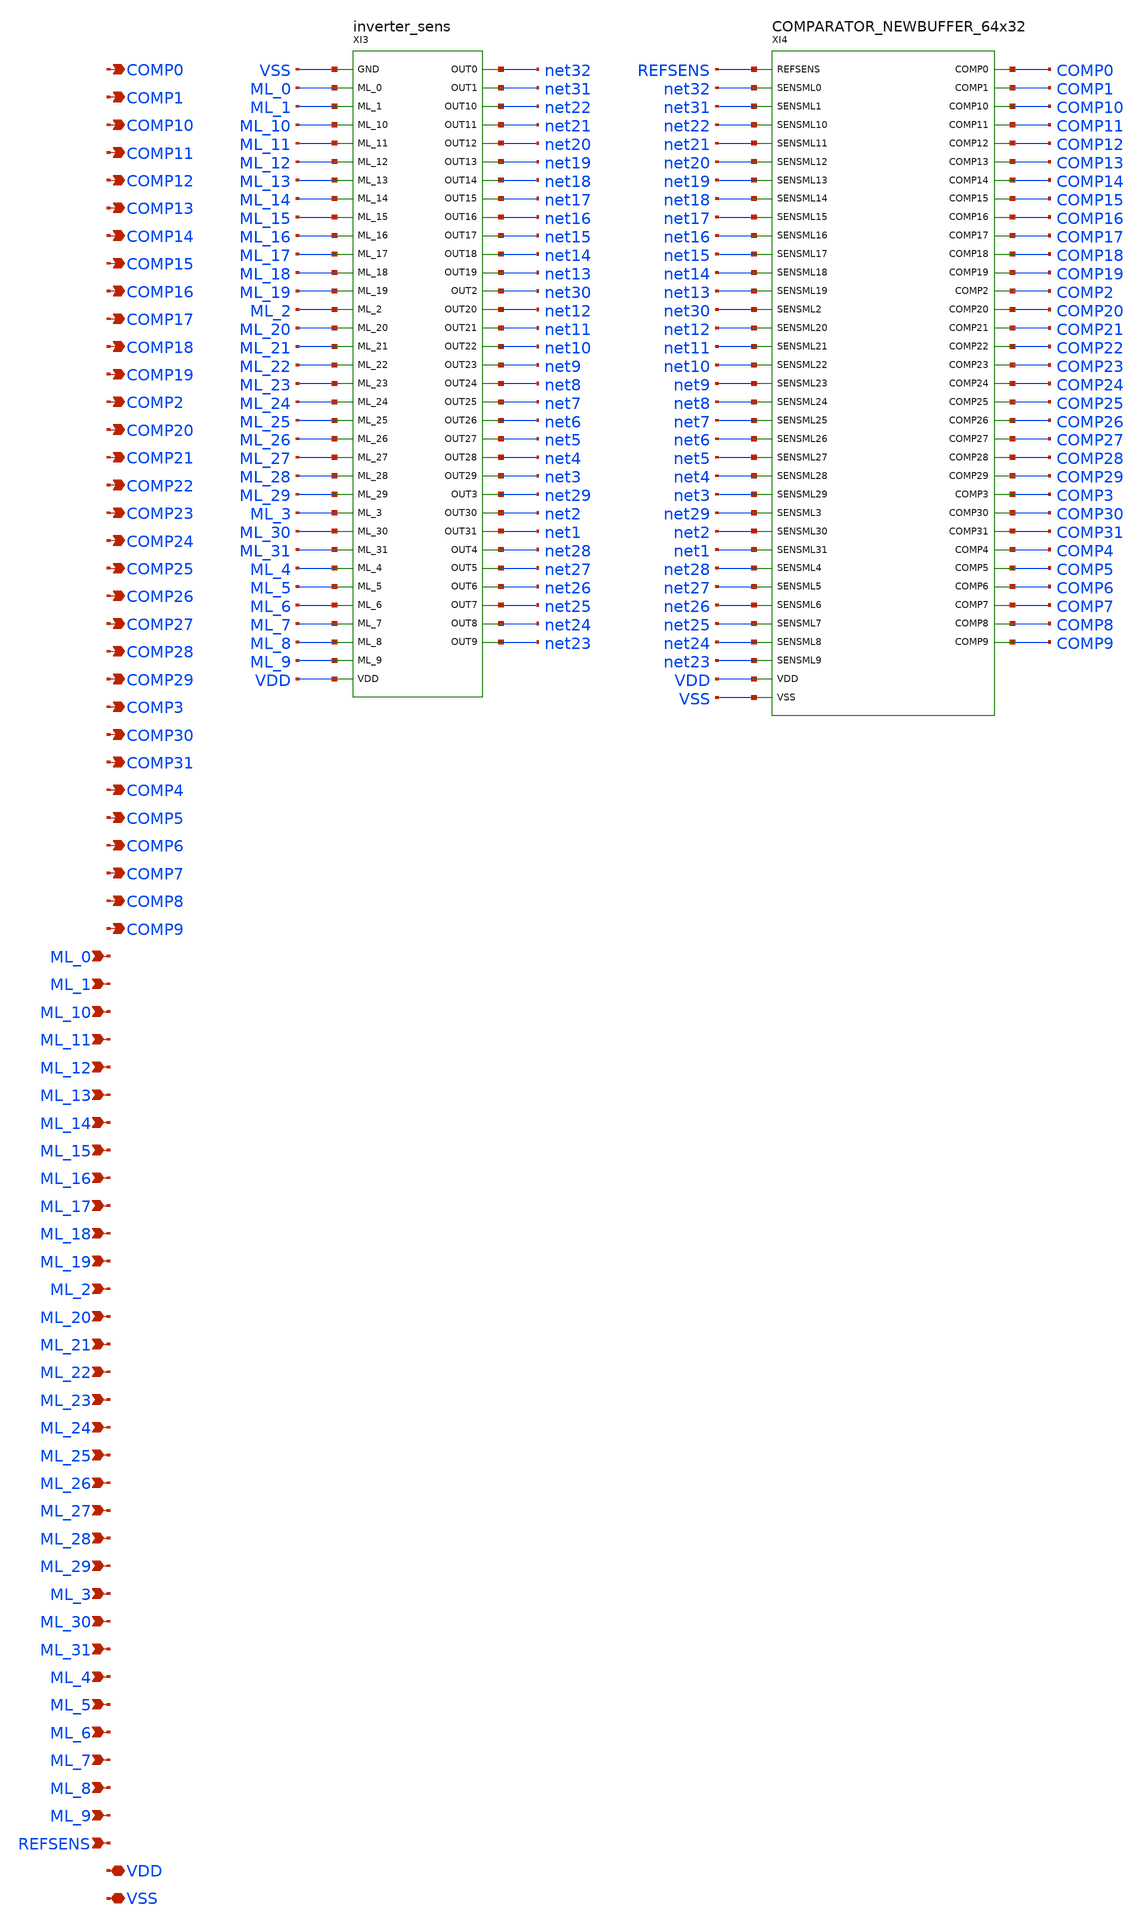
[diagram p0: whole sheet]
** sch_path: SoC6169-main/schematic/xschem/PART_SENS_COMPARATOR.sch
* Copyright 2026 USFQ CAM team
* Licensed under the Apache License, Version 2.0 (the "License");
* you may not use this file except in compliance with the License.
* You may obtain a copy of the License at
* https://www.apache.org/licenses/LICENSE-2.0
* Unless required by applicable law or agreed to in writing, software
* distributed under the License is distributed on an "AS IS" BASIS,
* WITHOUT WARRANTIES OR CONDITIONS OF ANY KIND, either express or implied.
* See the License for the specific language governing permissions and
* limitations under the License.
**.subckt PART_SENS_COMPARATOR COMP0 COMP1 COMP10 COMP11 COMP12 COMP13 COMP14 COMP15 COMP16 COMP17
*+ COMP18 COMP19 COMP2 COMP20 COMP21 COMP22 COMP23 COMP24 COMP25 COMP26 COMP27 COMP28 COMP29 COMP3 COMP30
*+ COMP31 COMP4 COMP5 COMP6 COMP7 COMP8 COMP9 ML_0 ML_1 ML_10 ML_11 ML_12 ML_13 ML_14 ML_15 ML_16 ML_17 ML_18
*+ ML_19 ML_2 ML_20 ML_21 ML_22 ML_23 ML_24 ML_25 ML_26 ML_27 ML_28 ML_29 ML_3 ML_30 ML_31 ML_4 ML_5 ML_6
*+ ML_7 ML_8 ML_9 REFSENS VDD VSS
*.opin COMP0
*.opin COMP1
*.opin COMP10
*.opin COMP11
*.opin COMP12
*.opin COMP13
*.opin COMP14
*.opin COMP15
*.opin COMP16
*.opin COMP17
*.opin COMP18
*.opin COMP19
*.opin COMP2
*.opin COMP20
*.opin COMP21
*.opin COMP22
*.opin COMP23
*.opin COMP24
*.opin COMP25
*.opin COMP26
*.opin COMP27
*.opin COMP28
*.opin COMP29
*.opin COMP3
*.opin COMP30
*.opin COMP31
*.opin COMP4
*.opin COMP5
*.opin COMP6
*.opin COMP7
*.opin COMP8
*.opin COMP9
*.ipin ML_0
*.ipin ML_1
*.ipin ML_10
*.ipin ML_11
*.ipin ML_12
*.ipin ML_13
*.ipin ML_14
*.ipin ML_15
*.ipin ML_16
*.ipin ML_17
*.ipin ML_18
*.ipin ML_19
*.ipin ML_2
*.ipin ML_20
*.ipin ML_21
*.ipin ML_22
*.ipin ML_23
*.ipin ML_24
*.ipin ML_25
*.ipin ML_26
*.ipin ML_27
*.ipin ML_28
*.ipin ML_29
*.ipin ML_3
*.ipin ML_30
*.ipin ML_31
*.ipin ML_4
*.ipin ML_5
*.ipin ML_6
*.ipin ML_7
*.ipin ML_8
*.ipin ML_9
*.ipin REFSENS
*.iopin VDD
*.iopin VSS
XI3 VSS ML_0 ML_1 ML_10 ML_11 ML_12 ML_13 ML_14 ML_15 ML_16 ML_17 ML_18 ML_19 ML_2 ML_20 ML_21 ML_22
+ ML_23 ML_24 ML_25 ML_26 ML_27 ML_28 ML_29 ML_3 ML_30 ML_31 ML_4 ML_5 ML_6 ML_7 ML_8 ML_9 net32 net31
+ net22 net21 net20 net19 net18 net17 net16 net15 net14 net13 net30 net12 net11 net10 net9 net8 net7 net6
+ net5 net4 net3 net29 net2 net1 net28 net27 net26 net25 net24 net23 VDD inverter_sens
XI4 COMP0 COMP1 COMP10 COMP11 COMP12 COMP13 COMP14 COMP15 COMP16 COMP17 COMP18 COMP19 COMP2 COMP20
+ COMP21 COMP22 COMP23 COMP24 COMP25 COMP26 COMP27 COMP28 COMP29 COMP3 COMP30 COMP31 COMP4 COMP5 COMP6 COMP7
+ COMP8 COMP9 REFSENS net32 net31 net22 net21 net20 net19 net18 net17 net16 net15 net14 net13 net30 net12
+ net11 net10 net9 net8 net7 net6 net5 net4 net3 net29 net2 net1 net28 net27 net26 net25 net24 net23 VDD
+ VSS COMPARATOR_NEWBUFFER_64x32
**.ends

* expanding   symbol:  inverter_sens.sym # of pins=66
** sym_path: SoC6169-main/schematic/xschem/inverter_sens.sym
** sch_path: SoC6169-main/schematic/xschem/inverter_sens.sch
.subckt inverter_sens GND ML_0 ML_1 ML_10 ML_11 ML_12 ML_13 ML_14 ML_15 ML_16 ML_17 ML_18 ML_19 ML_2
+ ML_20 ML_21 ML_22 ML_23 ML_24 ML_25 ML_26 ML_27 ML_28 ML_29 ML_3 ML_30 ML_31 ML_4 ML_5 ML_6 ML_7 ML_8
+ ML_9 OUT0 OUT1 OUT10 OUT11 OUT12 OUT13 OUT14 OUT15 OUT16 OUT17 OUT18 OUT19 OUT2 OUT20 OUT21 OUT22 OUT23
+ OUT24 OUT25 OUT26 OUT27 OUT28 OUT29 OUT3 OUT30 OUT31 OUT4 OUT5 OUT6 OUT7 OUT8 OUT9 VDD
*.iopin GND
*.ipin ML_0
*.ipin ML_1
*.ipin ML_10
*.ipin ML_11
*.ipin ML_12
*.ipin ML_13
*.ipin ML_14
*.ipin ML_15
*.ipin ML_16
*.ipin ML_17
*.ipin ML_18
*.ipin ML_19
*.ipin ML_2
*.ipin ML_20
*.ipin ML_21
*.ipin ML_22
*.ipin ML_23
*.ipin ML_24
*.ipin ML_25
*.ipin ML_26
*.ipin ML_27
*.ipin ML_28
*.ipin ML_29
*.ipin ML_3
*.ipin ML_30
*.ipin ML_31
*.ipin ML_4
*.ipin ML_5
*.ipin ML_6
*.ipin ML_7
*.ipin ML_8
*.ipin ML_9
*.opin OUT0
*.opin OUT1
*.opin OUT10
*.opin OUT11
*.opin OUT12
*.opin OUT13
*.opin OUT14
*.opin OUT15
*.opin OUT16
*.opin OUT17
*.opin OUT18
*.opin OUT19
*.opin OUT2
*.opin OUT20
*.opin OUT21
*.opin OUT22
*.opin OUT23
*.opin OUT24
*.opin OUT25
*.opin OUT26
*.opin OUT27
*.opin OUT28
*.opin OUT29
*.opin OUT3
*.opin OUT30
*.opin OUT31
*.opin OUT4
*.opin OUT5
*.opin OUT6
*.opin OUT7
*.opin OUT8
*.opin OUT9
*.iopin VDD
XI33 GND ML_1 VDD OUT1 INV
XI32 GND ML_0 VDD OUT0 INV
XI60 GND ML_26 VDD OUT26 INV
XI58 GND ML_25 VDD OUT25 INV
XI38 GND ML_6 VDD OUT6 INV
XI59 GND ML_27 VDD OUT27 INV
XI41 GND ML_9 VDD OUT9 INV
XI35 GND ML_3 VDD OUT3 INV
XI51 GND ML_18 VDD OUT18 INV
XI50 GND ML_19 VDD OUT19 INV
XI49 GND ML_17 VDD OUT17 INV
XI44 GND ML_14 VDD OUT14 INV
XI46 GND ML_13 VDD OUT13 INV
XI48 GND ML_16 VDD OUT16 INV
XI47 GND ML_12 VDD OUT12 INV
XI34 GND ML_2 VDD OUT2 INV
XI55 GND ML_30 VDD OUT30 INV
XI57 GND ML_29 VDD OUT29 INV
XI56 GND ML_31 VDD OUT31 INV
XI37 GND ML_5 VDD OUT5 INV
XI40 GND ML_8 VDD OUT8 INV
XI43 GND ML_10 VDD OUT10 INV
XI52 GND ML_20 VDD OUT20 INV
XI54 GND ML_28 VDD OUT28 INV
XI53 GND ML_24 VDD OUT24 INV
XI61 GND ML_22 VDD OUT22 INV
XI36 GND ML_4 VDD OUT4 INV
XI63 GND ML_21 VDD OUT21 INV
XI62 GND ML_23 VDD OUT23 INV
XI39 GND ML_7 VDD OUT7 INV
XI42 GND ML_11 VDD OUT11 INV
XI45 GND ML_15 VDD OUT15 INV
.ends


* expanding   symbol:  COMPARATOR_NEWBUFFER_64x32.sym # of pins=67
** sym_path: SoC6169-main/schematic/xschem/COMPARATOR_NEWBUFFER_64x32.sym
** sch_path: SoC6169-main/schematic/xschem/COMPARATOR_NEWBUFFER_64x32.sch
.subckt COMPARATOR_NEWBUFFER_64x32 COMP0 COMP1 COMP10 COMP11 COMP12 COMP13 COMP14 COMP15 COMP16
+ COMP17 COMP18 COMP19 COMP2 COMP20 COMP21 COMP22 COMP23 COMP24 COMP25 COMP26 COMP27 COMP28 COMP29 COMP3
+ COMP30 COMP31 COMP4 COMP5 COMP6 COMP7 COMP8 COMP9 REFSENS SENSML0 SENSML1 SENSML10 SENSML11 SENSML12
+ SENSML13 SENSML14 SENSML15 SENSML16 SENSML17 SENSML18 SENSML19 SENSML2 SENSML20 SENSML21 SENSML22 SENSML23
+ SENSML24 SENSML25 SENSML26 SENSML27 SENSML28 SENSML29 SENSML3 SENSML30 SENSML31 SENSML4 SENSML5 SENSML6
+ SENSML7 SENSML8 SENSML9 VDD VSS
*.opin COMP0
*.opin COMP1
*.opin COMP10
*.opin COMP11
*.opin COMP12
*.opin COMP13
*.opin COMP14
*.opin COMP15
*.opin COMP16
*.opin COMP17
*.opin COMP18
*.opin COMP19
*.opin COMP2
*.opin COMP20
*.opin COMP21
*.opin COMP22
*.opin COMP23
*.opin COMP24
*.opin COMP25
*.opin COMP26
*.opin COMP27
*.opin COMP28
*.opin COMP29
*.opin COMP3
*.opin COMP30
*.opin COMP31
*.opin COMP4
*.opin COMP5
*.opin COMP6
*.opin COMP7
*.opin COMP8
*.opin COMP9
*.ipin REFSENS
*.ipin SENSML0
*.ipin SENSML1
*.ipin SENSML10
*.ipin SENSML11
*.ipin SENSML12
*.ipin SENSML13
*.ipin SENSML14
*.ipin SENSML15
*.ipin SENSML16
*.ipin SENSML17
*.ipin SENSML18
*.ipin SENSML19
*.ipin SENSML2
*.ipin SENSML20
*.ipin SENSML21
*.ipin SENSML22
*.ipin SENSML23
*.ipin SENSML24
*.ipin SENSML25
*.ipin SENSML26
*.ipin SENSML27
*.ipin SENSML28
*.ipin SENSML29
*.ipin SENSML3
*.ipin SENSML30
*.ipin SENSML31
*.ipin SENSML4
*.ipin SENSML5
*.ipin SENSML6
*.ipin SENSML7
*.ipin SENSML8
*.ipin SENSML9
*.iopin VDD
*.iopin VSS
XI36 REFSENS SENSML0 COMP0 net12 VDD VSS flip_flop
XI38 REFSENS SENSML2 COMP2 net11 VDD VSS flip_flop
XI37 REFSENS SENSML1 COMP1 net10 VDD VSS flip_flop
XI39 REFSENS SENSML3 COMP3 net9 VDD VSS flip_flop
XI40 REFSENS SENSML4 COMP4 net8 VDD VSS flip_flop
XI42 REFSENS SENSML6 COMP6 net7 VDD VSS flip_flop
XI41 REFSENS SENSML5 COMP5 net6 VDD VSS flip_flop
XI43 REFSENS SENSML7 COMP7 net5 VDD VSS flip_flop
XI44 REFSENS SENSML8 COMP8 net4 VDD VSS flip_flop
XI46 REFSENS SENSML10 COMP10 net3 VDD VSS flip_flop
XI45 REFSENS SENSML9 COMP9 net2 VDD VSS flip_flop
XI47 REFSENS SENSML11 COMP11 net1 VDD VSS flip_flop
XI48 REFSENS SENSML12 COMP12 net32 VDD VSS flip_flop
XI50 REFSENS SENSML14 COMP14 net31 VDD VSS flip_flop
XI49 REFSENS SENSML13 COMP13 net30 VDD VSS flip_flop
XI51 REFSENS SENSML15 COMP15 net29 VDD VSS flip_flop
XI52 REFSENS SENSML16 COMP16 net28 VDD VSS flip_flop
XI54 REFSENS SENSML19 COMP19 net27 VDD VSS flip_flop
XI53 REFSENS SENSML17 COMP17 net26 VDD VSS flip_flop
XI55 REFSENS SENSML18 COMP18 net25 VDD VSS flip_flop
XI56 REFSENS SENSML20 COMP20 net24 VDD VSS flip_flop
XI58 REFSENS SENSML22 COMP22 net23 VDD VSS flip_flop
XI57 REFSENS SENSML21 COMP21 net22 VDD VSS flip_flop
XI59 REFSENS SENSML23 COMP23 net21 VDD VSS flip_flop
XI60 REFSENS SENSML24 COMP24 net20 VDD VSS flip_flop
XI62 REFSENS SENSML26 COMP26 net19 VDD VSS flip_flop
XI61 REFSENS SENSML25 COMP25 net18 VDD VSS flip_flop
XI63 REFSENS SENSML27 COMP27 net17 VDD VSS flip_flop
XI64 REFSENS SENSML28 COMP28 net16 VDD VSS flip_flop
XI65 REFSENS SENSML29 COMP29 net15 VDD VSS flip_flop
XI66 REFSENS SENSML30 COMP30 net14 VDD VSS flip_flop
XI67 REFSENS SENSML31 COMP31 net13 VDD VSS flip_flop
.ends


* expanding   symbol:  INV.sym # of pins=4
** sym_path: SoC6169-main/schematic/xschem/INV.sym
** sch_path: SoC6169-main/schematic/xschem/INV.sch
.subckt INV GND IN VDD Y
*.iopin GND
*.ipin IN
*.iopin VDD
*.opin Y
XMN0 Y IN GND GND sg13_lv_nmos w=200n l=130n ng=1 m=1 mm_ok=1
XMP0 Y IN VDD VDD sg13_lv_pmos w=400n l=130n ng=1 m=1 mm_ok=1
.ends


* expanding   symbol:  flip_flop.sym # of pins=6
** sym_path: SoC6169-main/schematic/xschem/flip_flop.sym
** sch_path: SoC6169-main/schematic/xschem/flip_flop.sch
.subckt flip_flop CLK D Q Q_n VDD VSS
*.ipin CLK
*.ipin D
*.opin Q
*.opin Q_n
*.iopin VDD
*.iopin VSS
XI7 VSS Q_n VDD Q INV
XI5 VSS Q_n VDD net14 INV
XI4 VSS net17 VDD Q_n INV
XI3 VSS net9 VDD net15 INV
XI2 VSS CLK VDD net12 INV
XI1 VSS net8 VDD net9 INV
XI0 VSS D VDD net5 INV
XMN4 net17 net12 net14 VSS sg13_lv_nmos w=740n l=130n ng=1 m=1 mm_ok=1
XMN3 net9 CLK net17 VSS sg13_lv_nmos w=740n l=130n ng=1 m=1 mm_ok=1
XMN2 net8 CLK net15 VSS sg13_lv_nmos w=740n l=130n ng=1 m=1 mm_ok=1
XMN0 net5 net12 net8 VSS sg13_lv_nmos w=740n l=130n ng=1 m=1 mm_ok=1
XMP4 net17 CLK net14 VDD sg13_lv_pmos w=1120n l=130n ng=1 m=1 mm_ok=1
XMP3 net9 net12 net17 VDD sg13_lv_pmos w=1120n l=130n ng=1 m=1 mm_ok=1
XMP2 net8 net12 net15 VDD sg13_lv_pmos w=1120n l=130n ng=1 m=1 mm_ok=1
XMP0 net5 CLK net8 VDD sg13_lv_pmos w=1120n l=130n ng=1 m=1 mm_ok=1
.ends

.end
